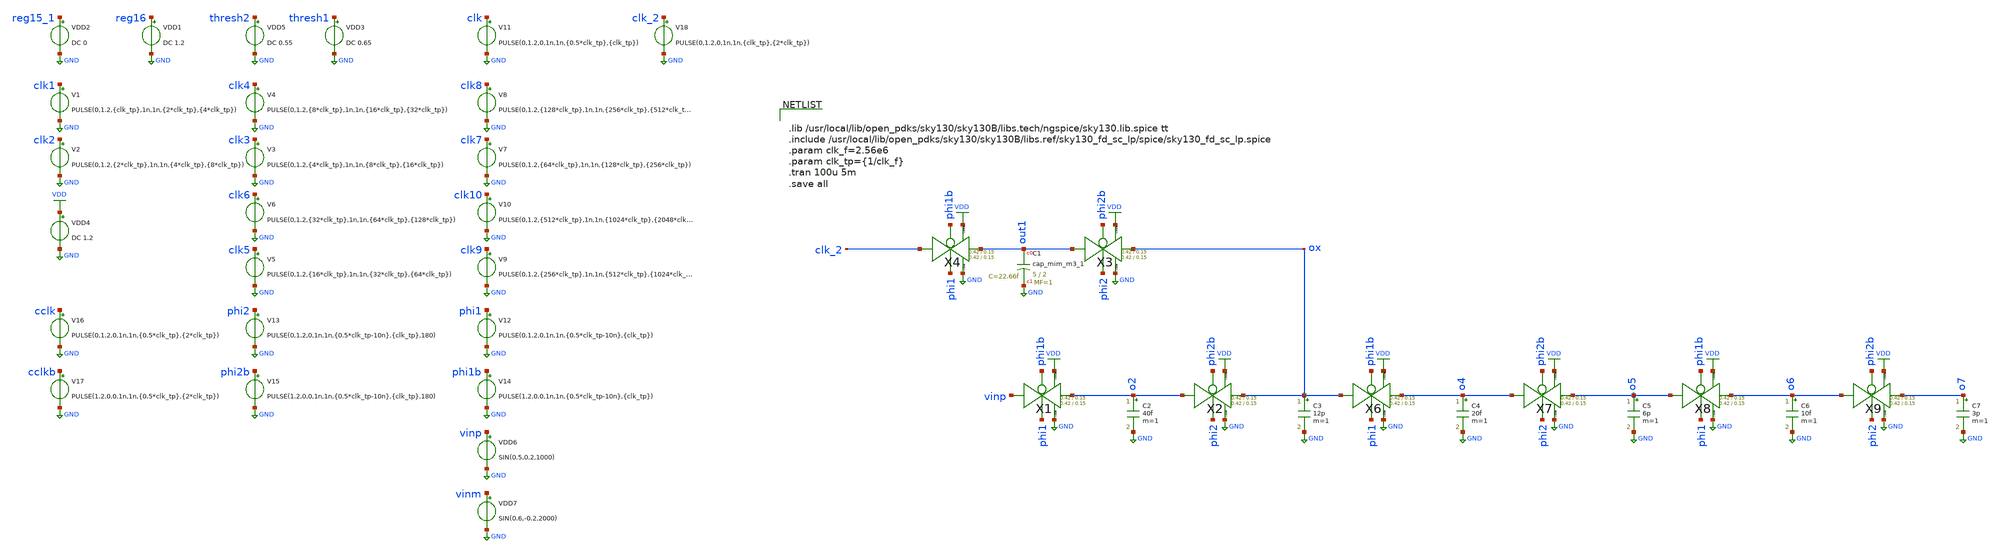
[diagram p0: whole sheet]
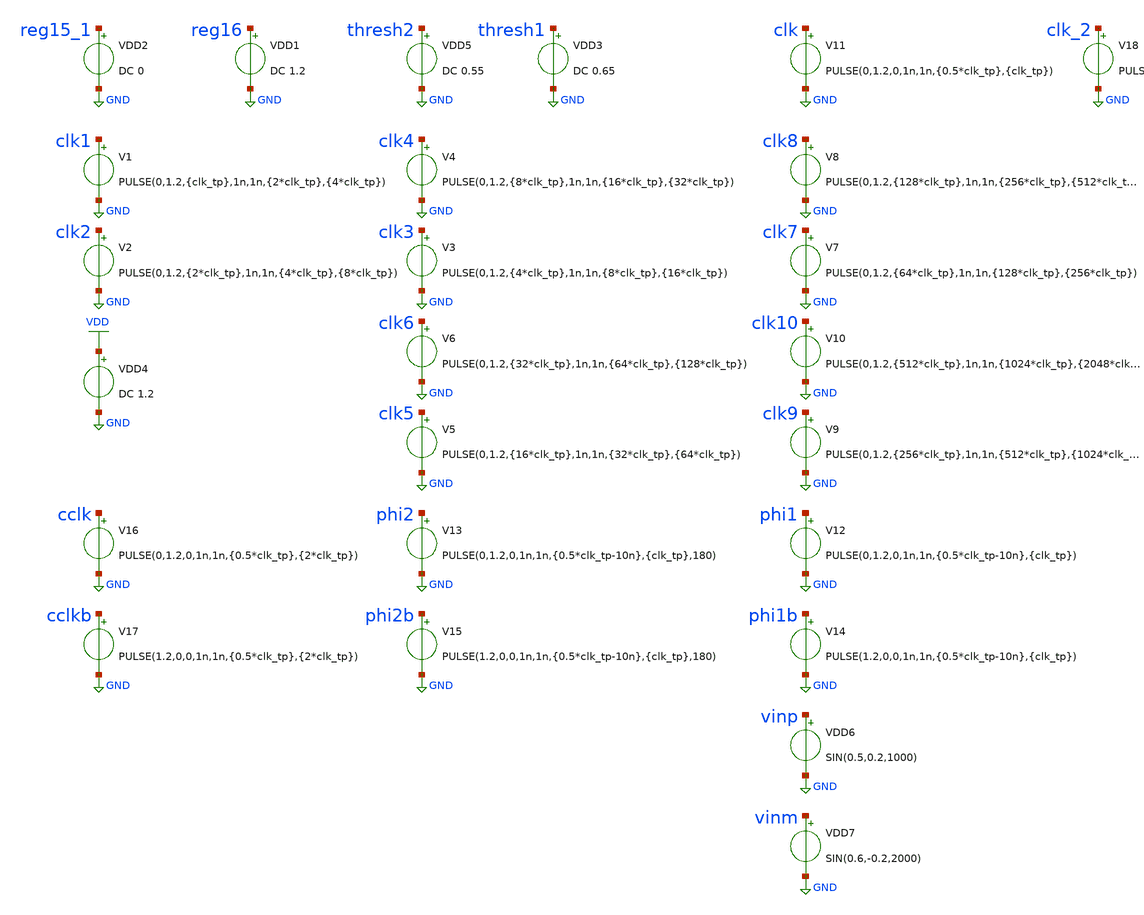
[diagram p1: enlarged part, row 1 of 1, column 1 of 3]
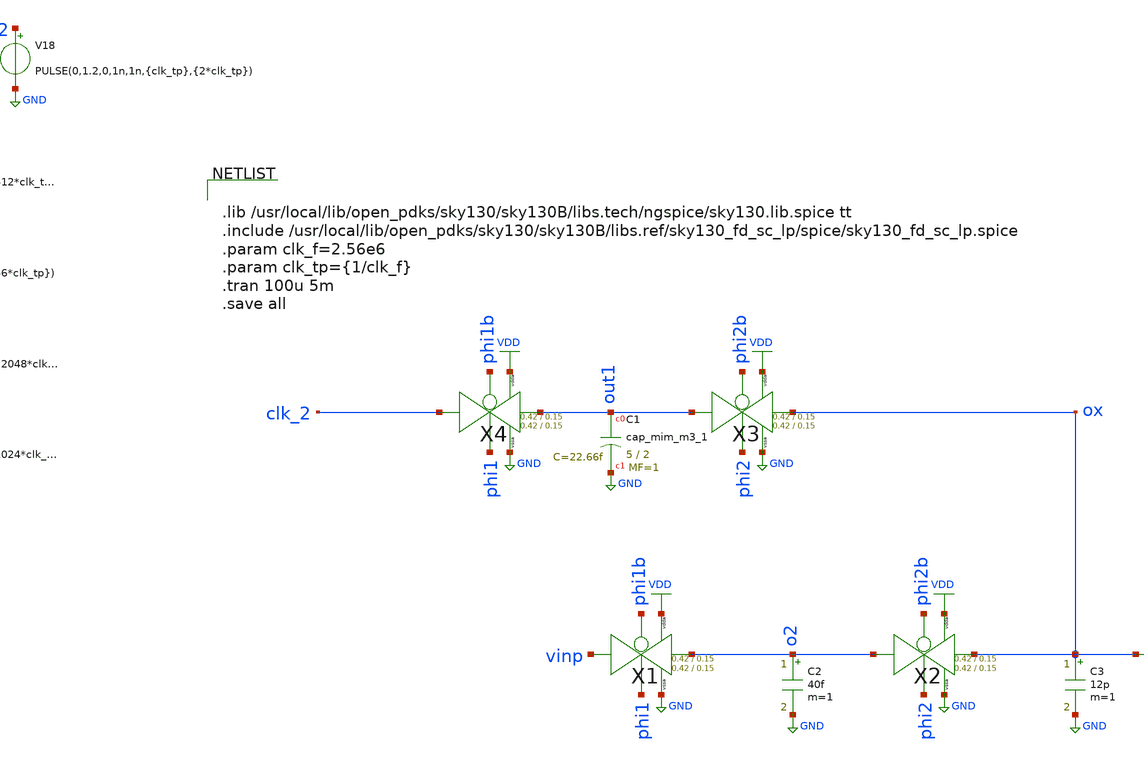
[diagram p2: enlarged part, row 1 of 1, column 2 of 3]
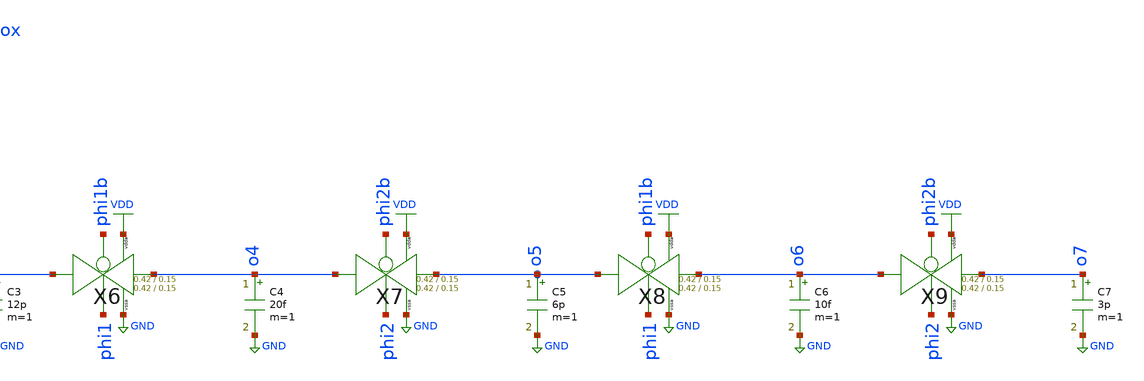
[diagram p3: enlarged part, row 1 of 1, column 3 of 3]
** sch_path: xschem/tryandtest/archive/feedback_check_no_clkgen.sch
**.subckt feedback_check_no_clkgen
V1 clk1 GND PULSE(0,1.2,{clk_tp},1n,1n,{2*clk_tp},{4*clk_tp})
VDD4 VDD GND DC 1.2
V2 clk2 GND PULSE(0,1.2,{2*clk_tp},1n,1n,{4*clk_tp},{8*clk_tp})
V3 clk3 GND PULSE(0,1.2,{4*clk_tp},1n,1n,{8*clk_tp},{16*clk_tp})
V4 clk4 GND PULSE(0,1.2,{8*clk_tp},1n,1n,{16*clk_tp},{32*clk_tp})
V5 clk5 GND PULSE(0,1.2,{16*clk_tp},1n,1n,{32*clk_tp},{64*clk_tp})
V6 clk6 GND PULSE(0,1.2,{32*clk_tp},1n,1n,{64*clk_tp},{128*clk_tp})
V7 clk7 GND PULSE(0,1.2,{64*clk_tp},1n,1n,{128*clk_tp},{256*clk_tp})
V8 clk8 GND PULSE(0,1.2,{128*clk_tp},1n,1n,{256*clk_tp},{512*clk_tp})
V9 clk9 GND PULSE(0,1.2,{256*clk_tp},1n,1n,{512*clk_tp},{1024*clk_tp})
V10 clk10 GND PULSE(0,1.2,{512*clk_tp},1n,1n,{1024*clk_tp},{2048*clk_tp})
VDD1 reg16 GND DC 1.2
VDD2 reg15_1 GND DC 0
V11 clk GND PULSE(0,1.2,0,1n,1n,{0.5*clk_tp},{clk_tp})
VDD3 thresh1 GND DC 0.65
VDD5 thresh2 GND DC 0.55
V12 phi1 GND PULSE(0,1.2,0,1n,1n,{0.5*clk_tp-10n},{clk_tp})
V13 phi2 GND PULSE(0,1.2,0,1n,1n,{0.5*clk_tp-10n},{clk_tp},180)
V14 phi1b GND PULSE(1.2,0,0,1n,1n,{0.5*clk_tp-10n},{clk_tp})
V15 phi2b GND PULSE(1.2,0,0,1n,1n,{0.5*clk_tp-10n},{clk_tp},180)
V16 cclk GND PULSE(0,1.2,0,1n,1n,{0.5*clk_tp},{2*clk_tp})
V17 cclkb GND PULSE(1.2,0,0,1n,1n,{0.5*clk_tp},{2*clk_tp})
VDD6 vinp GND SIN(0.5,0.2,1000)
VDD7 vinm GND SIN(0.6,-0.2,2000)
XC1 out1 GND sky130_fd_pr__cap_mim_m3_1 W=5 L=2 MF=1 m=1
X3 out1 ox phi2b phi2 VDD GND transmission_gate Wpmos=0.42 Lpmos=0.15 Wnmos=0.42 Lnmos=0.15
X4 clk_2 out1 phi1b phi1 VDD GND transmission_gate Wpmos=0.42 Lpmos=0.15 Wnmos=0.42 Lnmos=0.15
C2 o2 GND 40f m=1
X1 vinp o2 phi1b phi1 VDD GND transmission_gate Wpmos=0.42 Lpmos=0.15 Wnmos=0.42 Lnmos=0.15
X2 o2 ox phi2b phi2 VDD GND transmission_gate Wpmos=0.42 Lpmos=0.15 Wnmos=0.42 Lnmos=0.15
C3 ox GND 12p m=1
C4 o4 GND 20f m=1
X6 ox o4 phi1b phi1 VDD GND transmission_gate Wpmos=0.42 Lpmos=0.15 Wnmos=0.42 Lnmos=0.15
X7 o4 o5 phi2b phi2 VDD GND transmission_gate Wpmos=0.42 Lpmos=0.15 Wnmos=0.42 Lnmos=0.15
C5 o5 GND 6p m=1
C6 o6 GND 10f m=1
X8 o5 o6 phi1b phi1 VDD GND transmission_gate Wpmos=0.42 Lpmos=0.15 Wnmos=0.42 Lnmos=0.15
X9 o6 o7 phi2b phi2 VDD GND transmission_gate Wpmos=0.42 Lpmos=0.15 Wnmos=0.42 Lnmos=0.15
C7 o7 GND 3p m=1
V18 clk_2 GND PULSE(0,1.2,0,1n,1n,{clk_tp},{2*clk_tp})
**** begin user architecture code


.lib /usr/local/lib/open_pdks/sky130/sky130B/libs.tech/ngspice/sky130.lib.spice tt
.include /usr/local/lib/open_pdks/sky130/sky130B/libs.ref/sky130_fd_sc_lp/spice/sky130_fd_sc_lp.spice
.param clk_f=2.56e6
.param clk_tp={1/clk_f}
.tran 100u 5m
.save all


**** end user architecture code
**.ends

* expanding   symbol:  transmission_gate/transmission_gate.sym # of pins=6
** sym_path: xschem/transmission_gate/transmission_gate.sym
** sch_path: xschem/transmission_gate/transmission_gate.sch
.subckt transmission_gate in out ctrl_ ctrl vdda vssa  Wpmos=Wpmos Lpmos=Lpmos Wnmos=Wnmos
+ Lnmos=Lnmos
*.iopin in
*.iopin out
*.ipin ctrl_
*.ipin ctrl
*.ipin vdda
*.ipin vssa
XM1 out ctrl in vssa sky130_fd_pr__nfet_01v8 L=Lnmos W=Wnmos nf=1 ad='int((nf+1)/2) * W/nf * 0.29' as='int((nf+2)/2) * W/nf * 0.29'
+ pd='2*int((nf+1)/2) * (W/nf + 0.29)' ps='2*int((nf+2)/2) * (W/nf + 0.29)' nrd='0.29 / W' nrs='0.29 / W'
+ sa=0 sb=0 sd=0 mult=1 m=1
XM2 out ctrl_ in vdda sky130_fd_pr__pfet_01v8 L=Lpmos W=1.26 nf=1 ad='int((nf+1)/2) * W/nf * 0.29' as='int((nf+2)/2) * W/nf * 0.29'
+ pd='2*int((nf+1)/2) * (W/nf + 0.29)' ps='2*int((nf+2)/2) * (W/nf + 0.29)' nrd='0.29 / W' nrs='0.29 / W'
+ sa=0 sb=0 sd=0 mult=1 m=1
.ends

.GLOBAL GND
.GLOBAL VDD
.end
